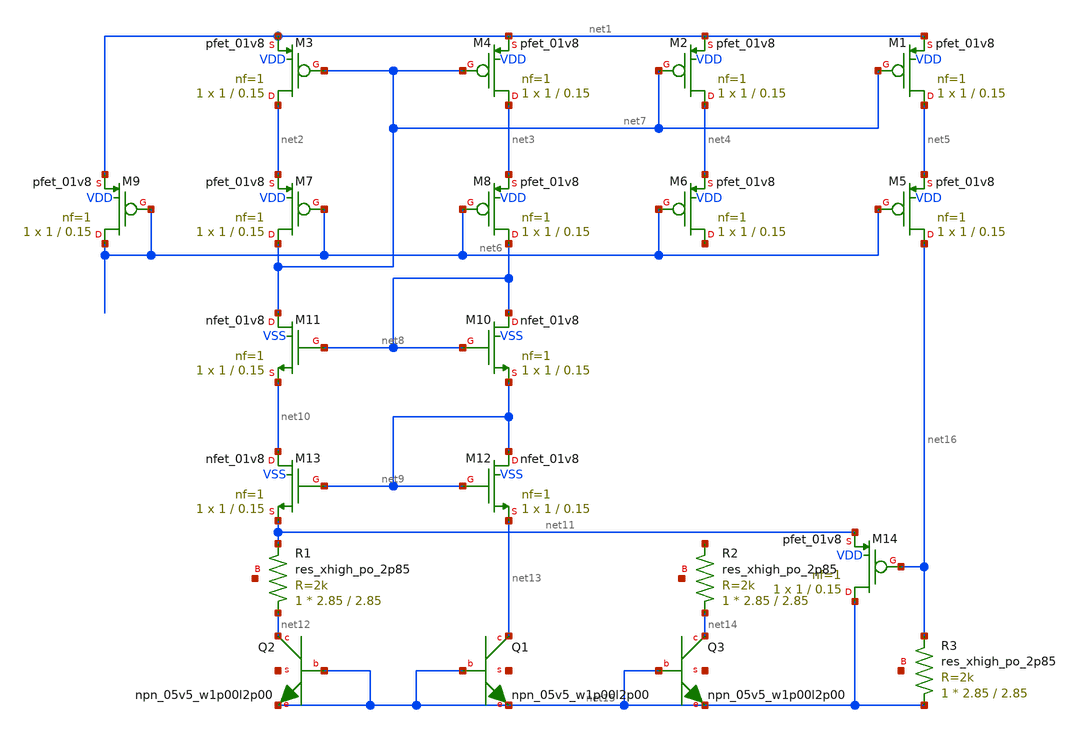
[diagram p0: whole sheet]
** sch_path: bandgap/bgr.sch
**.subckt bgr
XM1 net5 net7 net1 VDD sky130_fd_pr__pfet_01v8 L=0.15 W=1 nf=1 ad='int((nf+1)/2) * W/nf * 0.29' as='int((nf+2)/2) * W/nf * 0.29'
+ pd='2*int((nf+1)/2) * (W/nf + 0.29)' ps='2*int((nf+2)/2) * (W/nf + 0.29)' nrd='0.29 / W' nrs='0.29 / W'
+ sa=0 sb=0 sd=0 mult=1 m=1
XM2 net4 net7 net1 VDD sky130_fd_pr__pfet_01v8 L=0.15 W=1 nf=1 ad='int((nf+1)/2) * W/nf * 0.29' as='int((nf+2)/2) * W/nf * 0.29'
+ pd='2*int((nf+1)/2) * (W/nf + 0.29)' ps='2*int((nf+2)/2) * (W/nf + 0.29)' nrd='0.29 / W' nrs='0.29 / W'
+ sa=0 sb=0 sd=0 mult=1 m=1
XM3 net2 net7 net1 VDD sky130_fd_pr__pfet_01v8 L=0.15 W=1 nf=1 ad='int((nf+1)/2) * W/nf * 0.29' as='int((nf+2)/2) * W/nf * 0.29'
+ pd='2*int((nf+1)/2) * (W/nf + 0.29)' ps='2*int((nf+2)/2) * (W/nf + 0.29)' nrd='0.29 / W' nrs='0.29 / W'
+ sa=0 sb=0 sd=0 mult=1 m=1
XM4 net3 net7 net1 VDD sky130_fd_pr__pfet_01v8 L=0.15 W=1 nf=1 ad='int((nf+1)/2) * W/nf * 0.29' as='int((nf+2)/2) * W/nf * 0.29'
+ pd='2*int((nf+1)/2) * (W/nf + 0.29)' ps='2*int((nf+2)/2) * (W/nf + 0.29)' nrd='0.29 / W' nrs='0.29 / W'
+ sa=0 sb=0 sd=0 mult=1 m=1
XM5 net16 net6 net5 VDD sky130_fd_pr__pfet_01v8 L=0.15 W=1 nf=1 ad='int((nf+1)/2) * W/nf * 0.29' as='int((nf+2)/2) * W/nf * 0.29'
+ pd='2*int((nf+1)/2) * (W/nf + 0.29)' ps='2*int((nf+2)/2) * (W/nf + 0.29)' nrd='0.29 / W' nrs='0.29 / W'
+ sa=0 sb=0 sd=0 mult=1 m=1
XM6 net17 net6 net4 VDD sky130_fd_pr__pfet_01v8 L=0.15 W=1 nf=1 ad='int((nf+1)/2) * W/nf * 0.29' as='int((nf+2)/2) * W/nf * 0.29'
+ pd='2*int((nf+1)/2) * (W/nf + 0.29)' ps='2*int((nf+2)/2) * (W/nf + 0.29)' nrd='0.29 / W' nrs='0.29 / W'
+ sa=0 sb=0 sd=0 mult=1 m=1
XM7 net7 net6 net2 VDD sky130_fd_pr__pfet_01v8 L=0.15 W=1 nf=1 ad='int((nf+1)/2) * W/nf * 0.29' as='int((nf+2)/2) * W/nf * 0.29'
+ pd='2*int((nf+1)/2) * (W/nf + 0.29)' ps='2*int((nf+2)/2) * (W/nf + 0.29)' nrd='0.29 / W' nrs='0.29 / W'
+ sa=0 sb=0 sd=0 mult=1 m=1
XM8 net8 net6 net3 VDD sky130_fd_pr__pfet_01v8 L=0.15 W=1 nf=1 ad='int((nf+1)/2) * W/nf * 0.29' as='int((nf+2)/2) * W/nf * 0.29'
+ pd='2*int((nf+1)/2) * (W/nf + 0.29)' ps='2*int((nf+2)/2) * (W/nf + 0.29)' nrd='0.29 / W' nrs='0.29 / W'
+ sa=0 sb=0 sd=0 mult=1 m=1
XM9 net6 net6 net1 VDD sky130_fd_pr__pfet_01v8 L=0.15 W=1 nf=1 ad='int((nf+1)/2) * W/nf * 0.29' as='int((nf+2)/2) * W/nf * 0.29'
+ pd='2*int((nf+1)/2) * (W/nf + 0.29)' ps='2*int((nf+2)/2) * (W/nf + 0.29)' nrd='0.29 / W' nrs='0.29 / W'
+ sa=0 sb=0 sd=0 mult=1 m=1
XM10 net8 net8 net9 VSS sky130_fd_pr__nfet_01v8 L=0.15 W=1 nf=1 ad='int((nf+1)/2) * W/nf * 0.29' as='int((nf+2)/2) * W/nf * 0.29'
+ pd='2*int((nf+1)/2) * (W/nf + 0.29)' ps='2*int((nf+2)/2) * (W/nf + 0.29)' nrd='0.29 / W' nrs='0.29 / W'
+ sa=0 sb=0 sd=0 mult=1 m=1
XM11 net7 net8 net10 VSS sky130_fd_pr__nfet_01v8 L=0.15 W=1 nf=1 ad='int((nf+1)/2) * W/nf * 0.29' as='int((nf+2)/2) * W/nf * 0.29'
+ pd='2*int((nf+1)/2) * (W/nf + 0.29)' ps='2*int((nf+2)/2) * (W/nf + 0.29)' nrd='0.29 / W' nrs='0.29 / W'
+ sa=0 sb=0 sd=0 mult=1 m=1
XM12 net9 net9 net13 VSS sky130_fd_pr__nfet_01v8 L=0.15 W=1 nf=1 ad='int((nf+1)/2) * W/nf * 0.29' as='int((nf+2)/2) * W/nf * 0.29'
+ pd='2*int((nf+1)/2) * (W/nf + 0.29)' ps='2*int((nf+2)/2) * (W/nf + 0.29)' nrd='0.29 / W' nrs='0.29 / W'
+ sa=0 sb=0 sd=0 mult=1 m=1
XM13 net10 net9 net11 VSS sky130_fd_pr__nfet_01v8 L=0.15 W=1 nf=1 ad='int((nf+1)/2) * W/nf * 0.29' as='int((nf+2)/2) * W/nf * 0.29'
+ pd='2*int((nf+1)/2) * (W/nf + 0.29)' ps='2*int((nf+2)/2) * (W/nf + 0.29)' nrd='0.29 / W' nrs='0.29 / W'
+ sa=0 sb=0 sd=0 mult=1 m=1
XM14 net15 net16 net11 VDD sky130_fd_pr__pfet_01v8 L=0.15 W=1 nf=1 ad='int((nf+1)/2) * W/nf * 0.29' as='int((nf+2)/2) * W/nf * 0.29'
+ pd='2*int((nf+1)/2) * (W/nf + 0.29)' ps='2*int((nf+2)/2) * (W/nf + 0.29)' nrd='0.29 / W' nrs='0.29 / W'
+ sa=0 sb=0 sd=0 mult=1 m=1
XQ1 net13 net15 net15 net18 sky130_fd_pr__npn_05v5_w1p00l2p00
XQ2 net12 net15 net15 net19 sky130_fd_pr__npn_05v5_w1p00l2p00
XQ3 net14 net15 net15 net20 sky130_fd_pr__npn_05v5_w1p00l2p00
XR1 net12 net11 net21 sky130_fd_pr__res_xhigh_po_2p85 L=2.85 mult=1 m=1
XR2 net14 net22 net23 sky130_fd_pr__res_xhigh_po_2p85 L=2.85 mult=1 m=1
XR3 net15 net16 net24 sky130_fd_pr__res_xhigh_po_2p85 L=2.85 mult=1 m=1
**.ends
.end
